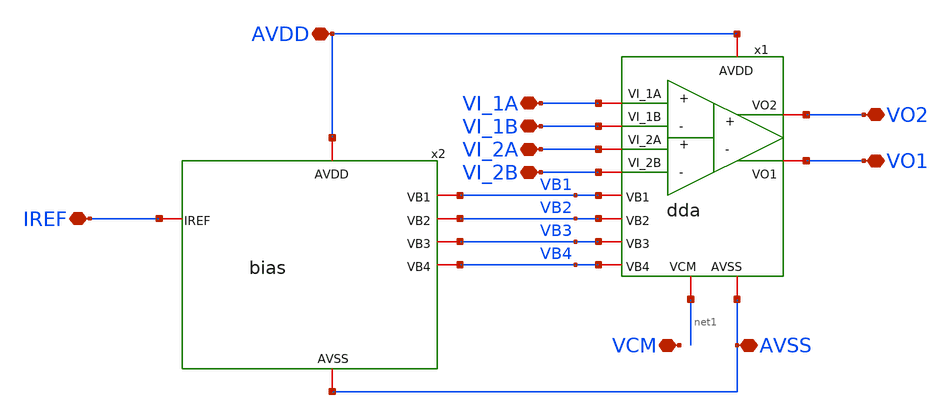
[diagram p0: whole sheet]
** sch_path: xschem/INA_layout_v2/ina_top.sch
**.subckt ina_top IREF VI_1A VI_1B VI_2A VI_2B VO2 VO1 VCM AVDD AVSS
*.iopin IREF
*.iopin VI_1A
*.iopin VI_1B
*.iopin VI_2A
*.iopin VI_2B
*.iopin VO2
*.iopin VO1
*.iopin VCM
*.iopin AVDD
*.iopin AVSS
x1 AVDD AVSS VI_1A VI_1B VO2 VO1 net1 VB1 VB2 VB3 VB4 VI_2A VI_2B dda
x2 IREF VB1 AVDD AVSS VB2 VB3 VB4 bias
**.ends
.end
